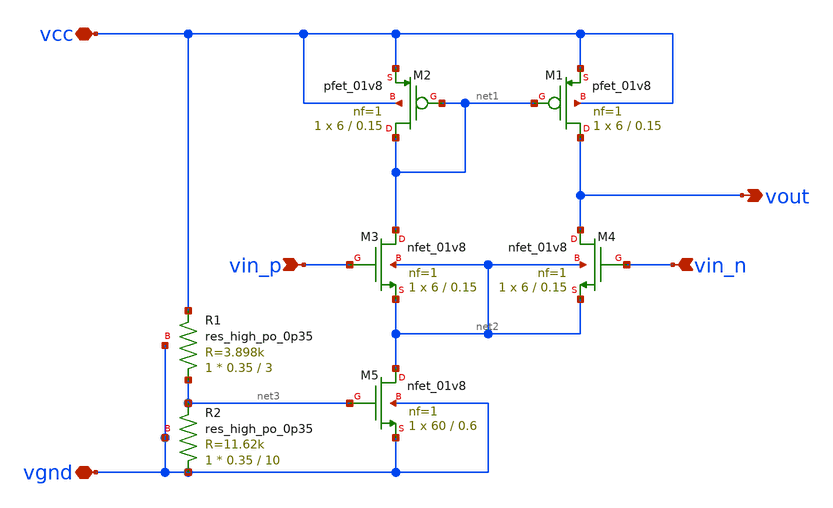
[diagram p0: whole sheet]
** sch_path: xschem/a1_opamp.sch
**.subckt a1_opamp vin_p vin_n vout vcc vgnd
*.ipin vin_p
*.ipin vin_n
*.opin vout
*.iopin vcc
*.iopin vgnd
XM1 vout net1 vcc vcc sky130_fd_pr__pfet_01v8 L=0.15 W=6 nf=1 ad='int((nf+1)/2) * W/nf * 0.29' as='int((nf+2)/2) * W/nf * 0.29'
+ pd='2*int((nf+1)/2) * (W/nf + 0.29)' ps='2*int((nf+2)/2) * (W/nf + 0.29)' nrd='0.29 / W' nrs='0.29 / W'
+ sa=0 sb=0 sd=0 mult=1 m=1
XM2 net1 net1 vcc vcc sky130_fd_pr__pfet_01v8 L=0.15 W=6 nf=1 ad='int((nf+1)/2) * W/nf * 0.29' as='int((nf+2)/2) * W/nf * 0.29'
+ pd='2*int((nf+1)/2) * (W/nf + 0.29)' ps='2*int((nf+2)/2) * (W/nf + 0.29)' nrd='0.29 / W' nrs='0.29 / W'
+ sa=0 sb=0 sd=0 mult=1 m=1
XM3 net1 vin_p net2 net2 sky130_fd_pr__nfet_01v8 L=0.15 W=6 nf=1 ad='int((nf+1)/2) * W/nf * 0.29' as='int((nf+2)/2) * W/nf * 0.29'
+ pd='2*int((nf+1)/2) * (W/nf + 0.29)' ps='2*int((nf+2)/2) * (W/nf + 0.29)' nrd='0.29 / W' nrs='0.29 / W'
+ sa=0 sb=0 sd=0 mult=1 m=1
XM4 vout vin_n net2 net2 sky130_fd_pr__nfet_01v8 L=0.15 W=6 nf=1 ad='int((nf+1)/2) * W/nf * 0.29' as='int((nf+2)/2) * W/nf * 0.29'
+ pd='2*int((nf+1)/2) * (W/nf + 0.29)' ps='2*int((nf+2)/2) * (W/nf + 0.29)' nrd='0.29 / W' nrs='0.29 / W'
+ sa=0 sb=0 sd=0 mult=1 m=1
XM5 net2 net3 vgnd vgnd sky130_fd_pr__nfet_01v8 L=0.6 W=60 nf=1 ad='int((nf+1)/2) * W/nf * 0.29' as='int((nf+2)/2) * W/nf * 0.29'
+ pd='2*int((nf+1)/2) * (W/nf + 0.29)' ps='2*int((nf+2)/2) * (W/nf + 0.29)' nrd='0.29 / W' nrs='0.29 / W'
+ sa=0 sb=0 sd=0 mult=1 m=1
XR1 net3 vcc vgnd sky130_fd_pr__res_high_po_0p35 L=3 mult=1 m=1
XR2 vgnd net3 vgnd sky130_fd_pr__res_high_po_0p35 L=10 mult=1 m=1
**.ends
.end
